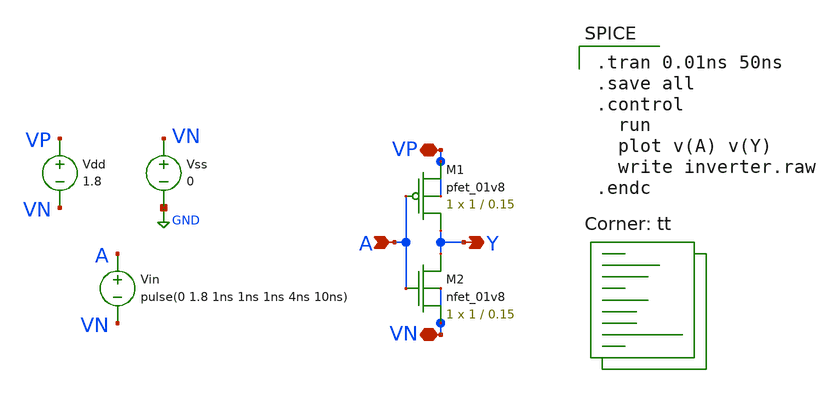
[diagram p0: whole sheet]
** sch_path: DAC/inverter.sch
**.subckt inverter A Y VN VP
*.ipin A
*.opin Y
*.iopin VN
*.iopin VP
Vdd VP VN 1.8
Vin A VN pulse(0 1.8 1ns 1ns 1ns 4ns 10ns)
XM2 Y A VN VN sky130_fd_pr__nfet_01v8 L=0.15 W=1 nf=1 ad='int((nf+1)/2) * W/nf * 0.29' as='int((nf+2)/2) * W/nf * 0.29'
+ pd='2*int((nf+1)/2) * (W/nf + 0.29)' ps='2*int((nf+2)/2) * (W/nf + 0.29)' nrd='0.29 / W' nrs='0.29 / W'
+ sa=0 sb=0 sd=0 mult=1 m=1
XM1 Y A VP VP sky130_fd_pr__pfet_01v8 L=0.15 W=1 nf=1 ad='int((nf+1)/2) * W/nf * 0.29' as='int((nf+2)/2) * W/nf * 0.29'
+ pd='2*int((nf+1)/2) * (W/nf + 0.29)' ps='2*int((nf+2)/2) * (W/nf + 0.29)' nrd='0.29 / W' nrs='0.29 / W'
+ sa=0 sb=0 sd=0 mult=1 m=1
Vss VN GND 0
**** begin user architecture code

.tran 0.01ns 50ns
.save all
.control
  run
  plot v(A) v(Y)
  write inverter.raw
.endc

.lib $::SKYWATER_MODELS/sky130.lib.spice tt
**** end user architecture code
**.ends
.GLOBAL GND
.end
